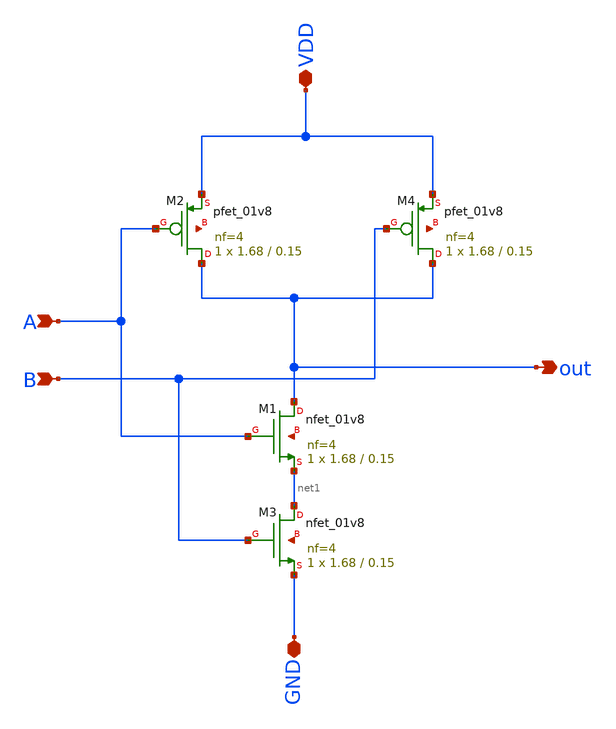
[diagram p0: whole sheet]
** sch_path: assignments/assignment5/nand.sch
**.subckt nand A out VDD GND B
*.ipin A
*.opin out
*.iopin VDD
*.iopin GND
*.ipin B
XM1 out A net1 net2 sky130_fd_pr__nfet_01v8 L=0.15 W=1.68 nf=4 ad='int((nf+1)/2) * W/nf * 0.29' as='int((nf+2)/2) * W/nf * 0.29'
+ pd='2*int((nf+1)/2) * (W/nf + 0.29)' ps='2*int((nf+2)/2) * (W/nf + 0.29)' nrd='0.29 / W' nrs='0.29 / W'
+ sa=0 sb=0 sd=0 mult=1 m=1
XM2 out A VDD net3 sky130_fd_pr__pfet_01v8 L=0.15 W=1.68 nf=4 ad='int((nf+1)/2) * W/nf * 0.29' as='int((nf+2)/2) * W/nf * 0.29'
+ pd='2*int((nf+1)/2) * (W/nf + 0.29)' ps='2*int((nf+2)/2) * (W/nf + 0.29)' nrd='0.29 / W' nrs='0.29 / W'
+ sa=0 sb=0 sd=0 mult=1 m=1
XM3 net1 B GND net4 sky130_fd_pr__nfet_01v8 L=0.15 W=1.68 nf=4 ad='int((nf+1)/2) * W/nf * 0.29' as='int((nf+2)/2) * W/nf * 0.29'
+ pd='2*int((nf+1)/2) * (W/nf + 0.29)' ps='2*int((nf+2)/2) * (W/nf + 0.29)' nrd='0.29 / W' nrs='0.29 / W'
+ sa=0 sb=0 sd=0 mult=1 m=1
XM4 out B VDD net5 sky130_fd_pr__pfet_01v8 L=0.15 W=1.68 nf=4 ad='int((nf+1)/2) * W/nf * 0.29' as='int((nf+2)/2) * W/nf * 0.29'
+ pd='2*int((nf+1)/2) * (W/nf + 0.29)' ps='2*int((nf+2)/2) * (W/nf + 0.29)' nrd='0.29 / W' nrs='0.29 / W'
+ sa=0 sb=0 sd=0 mult=1 m=1
**.ends
.end
